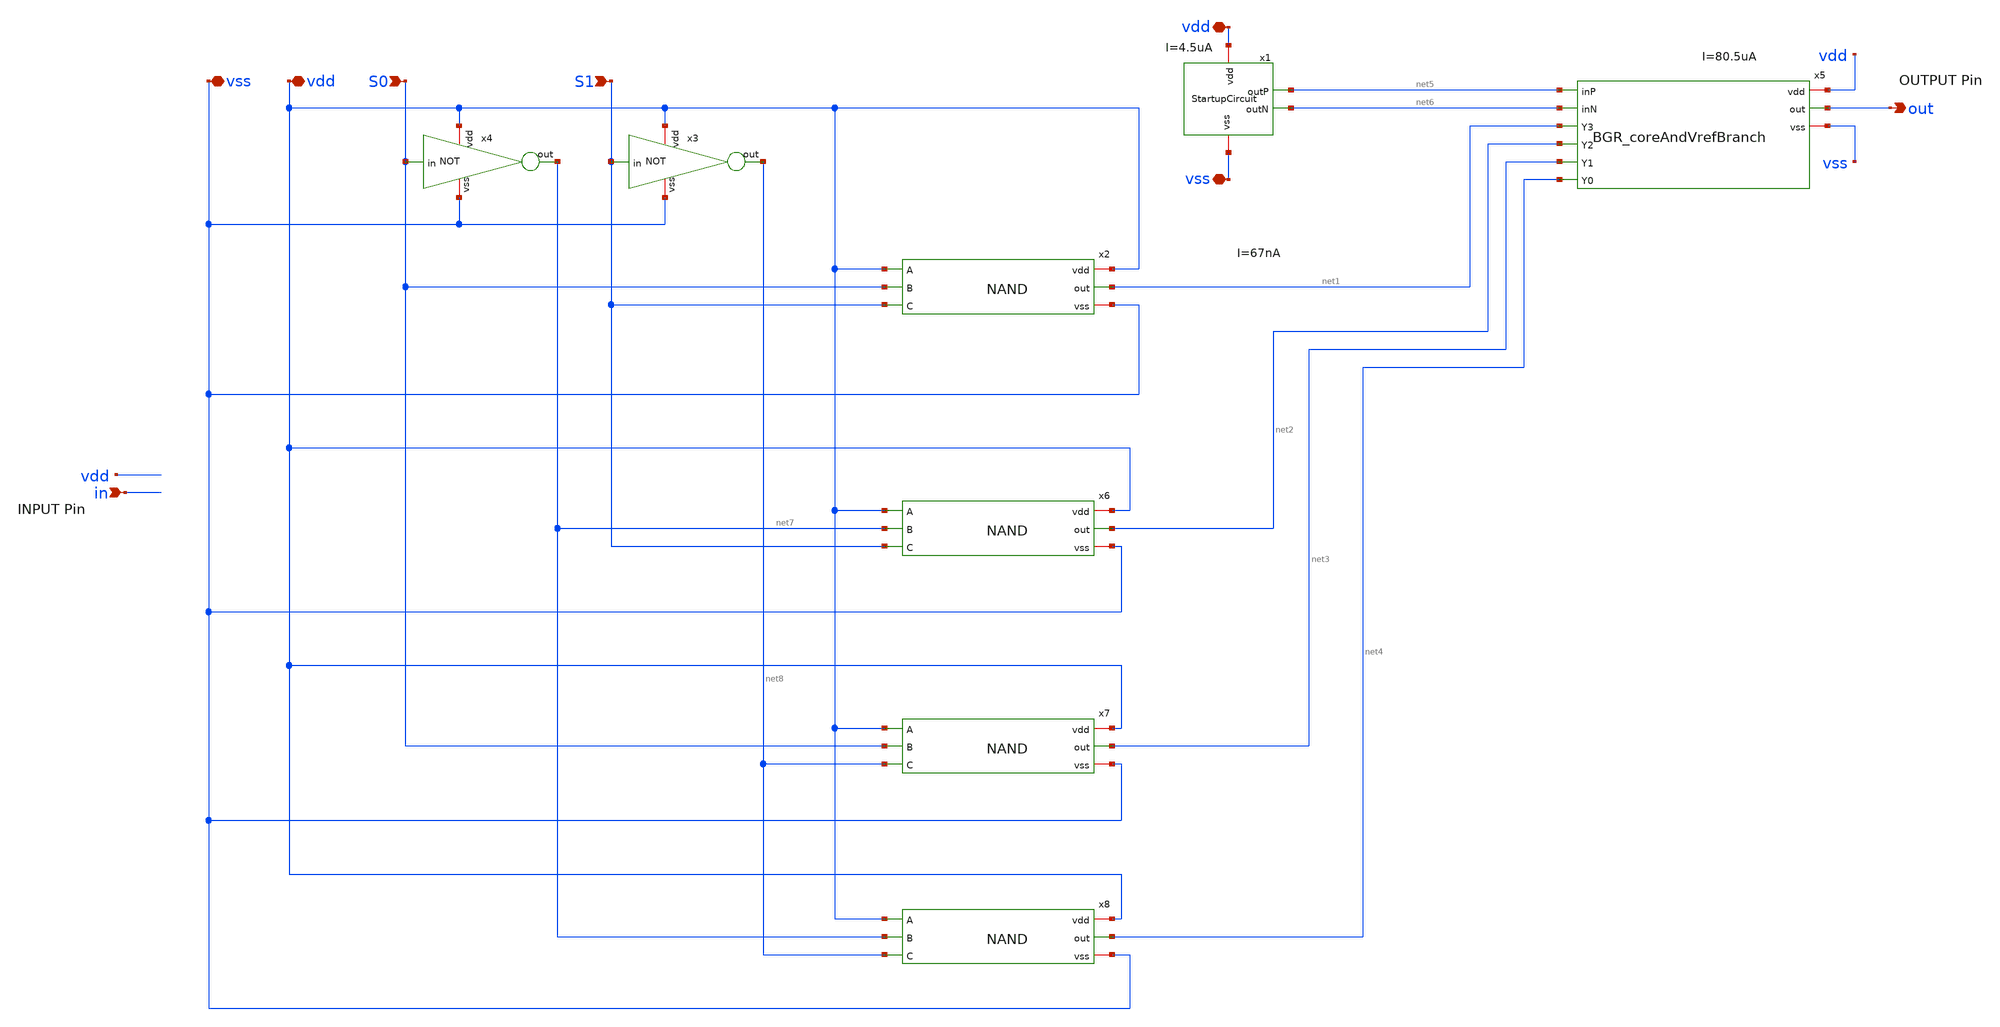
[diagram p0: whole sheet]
** sch_path: BGR_TOP_SKY130A/untitled-3.sch
**.subckt untitled-3 vdd out vss in S0 S1 vdd vss
*.iopin vdd
*.opin out
*.iopin vss
*.ipin in
*.ipin S0
*.ipin S1
*.iopin vdd
*.iopin vss
x1 vdd net5 net6 vss StartupCircuit
x5 vdd net5 net6 out net1 net2 net3 net4 vss BGR_coreAndVrefBranch
x2 vdd net1 vdd S0 S1 vss NAND
x3 vdd S1 net8 vss NOT
x4 vdd S0 net7 vss NOT
x6 vdd net2 vdd net7 S1 vss NAND
x7 vdd net3 vdd S0 net8 vss NAND
x8 vdd net4 vdd net7 net8 vss NAND
**.ends

* expanding   symbol:  StartupCircuit.sym # of pins=4
** sym_path: BGR_TOP_SKY130A/StartupCircuit.sym
** sch_path: BGR_TOP_SKY130A/StartupCircuit.sch
.subckt StartupCircuit vdd outP outN vss
*.iopin vdd
*.iopin vss
*.opin outP
*.opin outN
XM4 net2 outP vdd vdd sky130_fd_pr__pfet_01v8_lvt L=1 W=2 nf=1 ad='int((1 + 1)/2) * 2 / 1 * 0.29' as='int((1 + 2)/2) * 2 / 1 * 0.29'
+ pd='2*int((1 + 1)/2) * (2 / 1 + 0.29)' ps='2*int((1 + 2)/2) * (2 / 1 + 0.29)' nrd='0.29 / 2 ' nrs='0.29 / 2 '
+ sa=0 sb=0 sd=0 mult=1 m=1
XM7 outN net1 outP vdd sky130_fd_pr__pfet_01v8_lvt L=1 W=2 nf=1 ad='int((1 + 1)/2) * 2 / 1 * 0.29' as='int((1 + 2)/2) * 2 / 1 * 0.29'
+ pd='2*int((1 + 1)/2) * (2 / 1 + 0.29)' ps='2*int((1 + 2)/2) * (2 / 1 + 0.29)' nrd='0.29 / 2 ' nrs='0.29 / 2 '
+ sa=0 sb=0 sd=0 mult=2 m=2
XM9 net1 net1 net3 vss sky130_fd_pr__nfet_01v8_lvt L=1 W=1 nf=1 ad='int((1 + 1)/2) * 1 / 1 * 0.29' as='int((1 + 2)/2) * 1 / 1 * 0.29'
+ pd='2*int((1 + 1)/2) * (1 / 1 + 0.29)' ps='2*int((1 + 2)/2) * (1 / 1 + 0.29)' nrd='0.29 / 1 ' nrs='0.29 / 1 '
+ sa=0 sb=0 sd=0 mult=1 m=1
XM5 net1 outP net2 vdd sky130_fd_pr__pfet_01v8_lvt L=1 W=2 nf=1 ad='int((1 + 1)/2) * 2 / 1 * 0.29' as='int((1 + 2)/2) * 2 / 1 * 0.29'
+ pd='2*int((1 + 1)/2) * (2 / 1 + 0.29)' ps='2*int((1 + 2)/2) * (2 / 1 + 0.29)' nrd='0.29 / 2 ' nrs='0.29 / 2 '
+ sa=0 sb=0 sd=0 mult=1 m=1
XM10 net3 net3 vss vss sky130_fd_pr__nfet_01v8_lvt L=1 W=1 nf=1 ad='int((1 + 1)/2) * 1 / 1 * 0.29' as='int((1 + 2)/2) * 1 / 1 * 0.29'
+ pd='2*int((1 + 1)/2) * (1 / 1 + 0.29)' ps='2*int((1 + 2)/2) * (1 / 1 + 0.29)' nrd='0.29 / 1 ' nrs='0.29 / 1 '
+ sa=0 sb=0 sd=0 mult=1 m=1
.ends


* expanding   symbol:  BGR_coreAndVrefBranch.sym # of pins=9
** sym_path: BGR_coreAndVrefBranch.sym
** sch_path: BGR_coreAndVrefBranch.sch
.subckt BGR_coreAndVrefBranch vdd inP inN out Y3 Y2 Y1 Y0 vss
*.opin out
*.iopin vss
*.ipin Y3
*.ipin Y2
*.ipin Y1
*.ipin Y0
*.iopin vdd
*.ipin inP
*.ipin inN
XM3 out net1 vdd vdd sky130_fd_pr__pfet_01v8_lvt L=2 W=3.2 nf=1 ad='int((1 + 1)/2) * 3.2 / 1 * 0.29'
+ as='int((1 + 2)/2) * 3.2 / 1 * 0.29' pd='2*int((1 + 1)/2) * (3.2 / 1 + 0.29)' ps='2*int((1 + 2)/2) * (3.2 / 1 + 0.29)'
+ nrd='0.29 / 3.2 ' nrs='0.29 / 3.2 ' sa=0 sb=0 sd=0 mult=4 m=4
XQ3 vss vss net2 sky130_fd_pr__pnp_05v5_W3p40L3p40 m=8
XR2 net2 net4 vss sky130_fd_pr__res_high_po W=0.22 L=8 mult=1 m=1
XM11 net4 Y3 out vdd sky130_fd_pr__pfet_01v8_lvt L=1 W=5 nf=1 ad='int((1 + 1)/2) * 5 / 1 * 0.29' as='int((1 + 2)/2) * 5 / 1 * 0.29'
+ pd='2*int((1 + 1)/2) * (5 / 1 + 0.29)' ps='2*int((1 + 2)/2) * (5 / 1 + 0.29)' nrd='0.29 / 5 ' nrs='0.29 / 5 '
+ sa=0 sb=0 sd=0 mult=8 m=8
XM12 net4 Y2 net5 vdd sky130_fd_pr__pfet_01v8_lvt L=1 W=5 nf=1 ad='int((1 + 1)/2) * 5 / 1 * 0.29' as='int((1 + 2)/2) * 5 / 1 * 0.29'
+ pd='2*int((1 + 1)/2) * (5 / 1 + 0.29)' ps='2*int((1 + 2)/2) * (5 / 1 + 0.29)' nrd='0.29 / 5 ' nrs='0.29 / 5 '
+ sa=0 sb=0 sd=0 mult=8 m=8
XM13 net4 Y1 net6 vdd sky130_fd_pr__pfet_01v8_lvt L=1 W=5 nf=1 ad='int((1 + 1)/2) * 5 / 1 * 0.29' as='int((1 + 2)/2) * 5 / 1 * 0.29'
+ pd='2*int((1 + 1)/2) * (5 / 1 + 0.29)' ps='2*int((1 + 2)/2) * (5 / 1 + 0.29)' nrd='0.29 / 5 ' nrs='0.29 / 5 '
+ sa=0 sb=0 sd=0 mult=8 m=8
XM14 net4 Y0 net3 vdd sky130_fd_pr__pfet_01v8_lvt L=1 W=5 nf=1 ad='int((1 + 1)/2) * 5 / 1 * 0.29' as='int((1 + 2)/2) * 5 / 1 * 0.29'
+ pd='2*int((1 + 1)/2) * (5 / 1 + 0.29)' ps='2*int((1 + 2)/2) * (5 / 1 + 0.29)' nrd='0.29 / 5 ' nrs='0.29 / 5 '
+ sa=0 sb=0 sd=0 mult=8 m=8
XR1 net3 net6 vss sky130_fd_pr__res_high_po W=1 L=0.5 mult=1 m=1
XR3 net6 net5 vss sky130_fd_pr__res_high_po W=2.304 L=0.5 mult=1 m=1
XR4 net5 out vss sky130_fd_pr__res_high_po W=2.147 L=0.5 mult=1 m=1
XM6 inN inN net9 vss sky130_fd_pr__nfet_01v8_lvt L=1 W=3.8 nf=1 ad='int((1 + 1)/2) * 3.8 / 1 * 0.29'
+ as='int((1 + 2)/2) * 3.8 / 1 * 0.29' pd='2*int((1 + 1)/2) * (3.8 / 1 + 0.29)' ps='2*int((1 + 2)/2) * (3.8 / 1 + 0.29)'
+ nrd='0.29 / 3.8 ' nrs='0.29 / 3.8 ' sa=0 sb=0 sd=0 mult=8 m=8
XM1 inN inP vdd vdd sky130_fd_pr__pfet_01v8_lvt L=2 W=3.2 nf=1 ad='int((1 + 1)/2) * 3.2 / 1 * 0.29' as='int((1 + 2)/2) * 3.2 / 1 * 0.29'
+ pd='2*int((1 + 1)/2) * (3.2 / 1 + 0.29)' ps='2*int((1 + 2)/2) * (3.2 / 1 + 0.29)' nrd='0.29 / 3.2 ' nrs='0.29 / 3.2 '
+ sa=0 sb=0 sd=0 mult=4 m=4
XQ1 vss vss net8 sky130_fd_pr__pnp_05v5_W3p40L3p40 m=8
XR5 net8 net7 vss sky130_fd_pr__res_high_po W=1.1 L=14.6 mult=1 m=1
XM2 net1 net1 vdd vdd sky130_fd_pr__pfet_01v8_lvt L=2 W=3.2 nf=1 ad='int((1 + 1)/2) * 3.2 / 1 * 0.29'
+ as='int((1 + 2)/2) * 3.2 / 1 * 0.29' pd='2*int((1 + 1)/2) * (3.2 / 1 + 0.29)' ps='2*int((1 + 2)/2) * (3.2 / 1 + 0.29)'
+ nrd='0.29 / 3.2 ' nrs='0.29 / 3.2 ' sa=0 sb=0 sd=0 mult=4 m=4
XM8 net1 inN net7 vss sky130_fd_pr__nfet_01v8_lvt L=1 W=3.8 nf=1 ad='int((1 + 1)/2) * 3.8 / 1 * 0.29'
+ as='int((1 + 2)/2) * 3.8 / 1 * 0.29' pd='2*int((1 + 1)/2) * (3.8 / 1 + 0.29)' ps='2*int((1 + 2)/2) * (3.8 / 1 + 0.29)'
+ nrd='0.29 / 3.8 ' nrs='0.29 / 3.8 ' sa=0 sb=0 sd=0 mult=8 m=8
XQ2 vss vss net10 sky130_fd_pr__pnp_05v5_W3p40L3p40 m=1
XR6 net10 net9 vss sky130_fd_pr__res_high_po W=2.28 L=14.6 mult=1 m=1
XR7 net1 inP vss sky130_fd_pr__res_high_po W=2000 L=0.01 mult=1000 m=1000
.ends


* expanding   symbol:  NAND.sym # of pins=6
** sym_path: NAND.sym
** sch_path: NAND.sch
.subckt NAND vdd out A B C vss
*.iopin vdd
*.iopin vss
*.ipin A
*.ipin C
*.ipin B
*.opin out
XM6 out A net1 vss sky130_fd_pr__nfet_01v8_lvt L=1 W=1 nf=1 ad='int((1 + 1)/2) * 1 / 1 * 0.29' as='int((1 + 2)/2) * 1 / 1 * 0.29'
+ pd='2*int((1 + 1)/2) * (1 / 1 + 0.29)' ps='2*int((1 + 2)/2) * (1 / 1 + 0.29)' nrd='0.29 / 1 ' nrs='0.29 / 1 '
+ sa=0 sb=0 sd=0 mult=2 m=2
XM1 out B vdd vdd sky130_fd_pr__pfet_01v8_lvt L=1 W=1 nf=1 ad='int((1 + 1)/2) * 1 / 1 * 0.29' as='int((1 + 2)/2) * 1 / 1 * 0.29'
+ pd='2*int((1 + 1)/2) * (1 / 1 + 0.29)' ps='2*int((1 + 2)/2) * (1 / 1 + 0.29)' nrd='0.29 / 1 ' nrs='0.29 / 1 '
+ sa=0 sb=0 sd=0 mult=4 m=4
XM2 out A vdd vdd sky130_fd_pr__pfet_01v8_lvt L=1 W=1 nf=1 ad='int((1 + 1)/2) * 1 / 1 * 0.29' as='int((1 + 2)/2) * 1 / 1 * 0.29'
+ pd='2*int((1 + 1)/2) * (1 / 1 + 0.29)' ps='2*int((1 + 2)/2) * (1 / 1 + 0.29)' nrd='0.29 / 1 ' nrs='0.29 / 1 '
+ sa=0 sb=0 sd=0 mult=4 m=4
XM3 net1 B net2 vss sky130_fd_pr__nfet_01v8_lvt L=1 W=1 nf=1 ad='int((1 + 1)/2) * 1 / 1 * 0.29' as='int((1 + 2)/2) * 1 / 1 * 0.29'
+ pd='2*int((1 + 1)/2) * (1 / 1 + 0.29)' ps='2*int((1 + 2)/2) * (1 / 1 + 0.29)' nrd='0.29 / 1 ' nrs='0.29 / 1 '
+ sa=0 sb=0 sd=0 mult=2 m=2
XM4 out C vdd vdd sky130_fd_pr__pfet_01v8_lvt L=1 W=1 nf=1 ad='int((1 + 1)/2) * 1 / 1 * 0.29' as='int((1 + 2)/2) * 1 / 1 * 0.29'
+ pd='2*int((1 + 1)/2) * (1 / 1 + 0.29)' ps='2*int((1 + 2)/2) * (1 / 1 + 0.29)' nrd='0.29 / 1 ' nrs='0.29 / 1 '
+ sa=0 sb=0 sd=0 mult=4 m=4
XM5 net2 C vss vss sky130_fd_pr__nfet_01v8_lvt L=1 W=1 nf=1 ad='int((1 + 1)/2) * 1 / 1 * 0.29' as='int((1 + 2)/2) * 1 / 1 * 0.29'
+ pd='2*int((1 + 1)/2) * (1 / 1 + 0.29)' ps='2*int((1 + 2)/2) * (1 / 1 + 0.29)' nrd='0.29 / 1 ' nrs='0.29 / 1 '
+ sa=0 sb=0 sd=0 mult=2 m=2
.ends


* expanding   symbol:  NOT.sym # of pins=4
** sym_path: BGR_TOP_SKY130A/NOT.sym
** sch_path: BGR_TOP_SKY130A/NOT.sch
.subckt NOT vdd in out vss
*.iopin vdd
*.iopin vss
*.ipin in
*.opin out
XM6 out in vss vss sky130_fd_pr__nfet_01v8_lvt L=1 W=1 nf=1 ad='int((1 + 1)/2) * 1 / 1 * 0.29' as='int((1 + 2)/2) * 1 / 1 * 0.29'
+ pd='2*int((1 + 1)/2) * (1 / 1 + 0.29)' ps='2*int((1 + 2)/2) * (1 / 1 + 0.29)' nrd='0.29 / 1 ' nrs='0.29 / 1 '
+ sa=0 sb=0 sd=0 mult=1 m=1
XM1 out in vdd vdd sky130_fd_pr__pfet_01v8_lvt L=1 W=1 nf=1 ad='int((1 + 1)/2) * 1 / 1 * 0.29' as='int((1 + 2)/2) * 1 / 1 * 0.29'
+ pd='2*int((1 + 1)/2) * (1 / 1 + 0.29)' ps='2*int((1 + 2)/2) * (1 / 1 + 0.29)' nrd='0.29 / 1 ' nrs='0.29 / 1 '
+ sa=0 sb=0 sd=0 mult=2 m=2
.ends

.end
